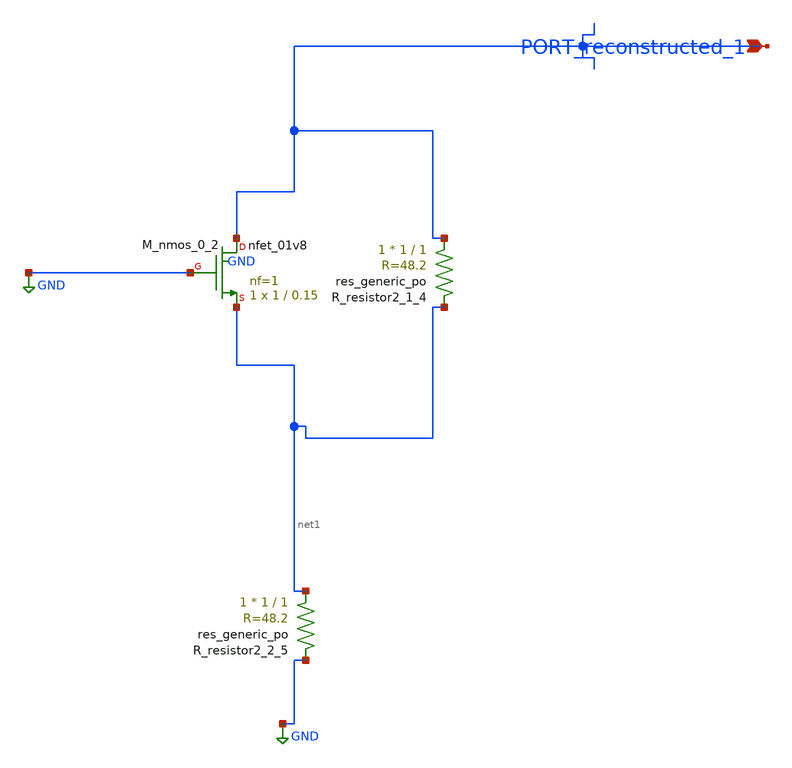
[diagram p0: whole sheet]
** sch_path: schematics/AMSNet/92.sch
**.subckt 92 PORT_reconstructed_1
*.ipin PORT_reconstructed_1
XM_nmos_0_2 PORT_reconstructed_1 GND net1 GND sky130_fd_pr__nfet_01v8 L=0.15 W=1 nf=1 ad='int((1 + 1)/2) * 1 / 1 * 0.29'
+ as='int((1 + 2)/2) * 1 / 1 * 0.29' pd='2*int((1 + 1)/2) * (1 / 1 + 0.29)' ps='2*int((1 + 2)/2) * (1 / 1 + 0.29)'
+ nrd='0.29 / 1 ' nrs='0.29 / 1 ' sa=0 sb=0 sd=0 mult=1 m=1
XR_resistor2_1_4 PORT_reconstructed_1 net1 sky130_fd_pr__res_generic_po W=1 L=1 m=1
XR_resistor2_2_5 net1 GND sky130_fd_pr__res_generic_po W=1 L=1 m=1
**.ends
.GLOBAL GND
.end
